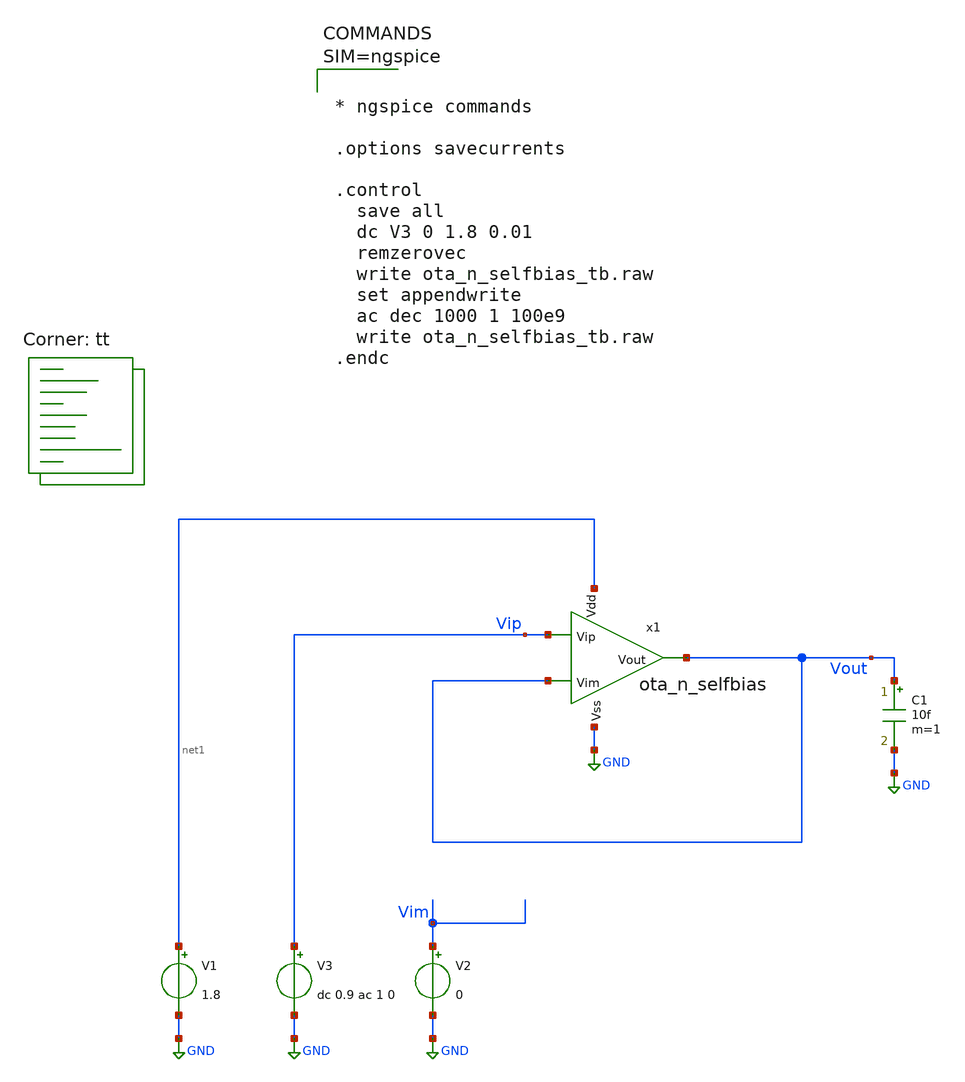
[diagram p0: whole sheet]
** sch_path: testbench/ota_n_selfbias_tb.sch
**.subckt ota_n_selfbias_tb
x1 net1 Vout Vout Vip GND ota_n_selfbias
V1 net1 GND 1.8
C1 Vout GND 10f m=1
V2 Vim GND 0
V3 Vip GND dc 0.9 ac 1 0
**** begin user architecture code
.lib $::SKYWATER_MODELS/sky130.lib.spice tt



* ngspice commands

.options savecurrents

.control
  save all
  dc V3 0 1.8 0.01
  remzerovec
  write ota_n_selfbias_tb.raw
  set appendwrite
  ac dec 1000 1 100e9
  write ota_n_selfbias_tb.raw
.endc



**** end user architecture code
**.ends

* expanding   symbol:  ota_n_selfbias.sym # of pins=5
** sym_path: schematic/ota_n_selfbias.sym
** sch_path: schematic/ota_n_selfbias.sch
.subckt ota_n_selfbias Vdd Vout Vim Vip Vss
*.ipin Vim
*.ipin Vip
*.opin Vout
*.ipin Vdd
*.ipin Vss
XM1 net1 Vim net3 Vss sky130_fd_pr__nfet_01v8_lvt L=0.4 W=1 nf=1 ad='int((1 + 1)/2) * 1 / 1 * 0.29' as='int((1 + 2)/2) * 1 / 1 * 0.29'
+ pd='2*int((1 + 1)/2) * (1 / 1 + 0.29)' ps='2*int((1 + 2)/2) * (1 / 1 + 0.29)' nrd='0.29 / 1 ' nrs='0.29 / 1 '
+ sa=0 sb=0 sd=0 mult=1 m=1
XM2 net2 Vip net3 Vss sky130_fd_pr__nfet_01v8_lvt L=0.4 W=1 nf=1 ad='int((1 + 1)/2) * 1 / 1 * 0.29' as='int((1 + 2)/2) * 1 / 1 * 0.29'
+ pd='2*int((1 + 1)/2) * (1 / 1 + 0.29)' ps='2*int((1 + 2)/2) * (1 / 1 + 0.29)' nrd='0.29 / 1 ' nrs='0.29 / 1 '
+ sa=0 sb=0 sd=0 mult=1 m=1
XM3 net3 net5 Vss Vss sky130_fd_pr__nfet_01v8_lvt L=0.4 W=1 nf=1 ad='int((1 + 1)/2) * 1 / 1 * 0.29' as='int((1 + 2)/2) * 1 / 1 * 0.29'
+ pd='2*int((1 + 1)/2) * (1 / 1 + 0.29)' ps='2*int((1 + 2)/2) * (1 / 1 + 0.29)' nrd='0.29 / 1 ' nrs='0.29 / 1 '
+ sa=0 sb=0 sd=0 mult=1 m=1
XM10 Vout net2 Vdd Vdd sky130_fd_pr__pfet_01v8_lvt L=0.4 W=1 nf=1 ad='int((1 + 1)/2) * 1 / 1 * 0.29'
+ as='int((1 + 2)/2) * 1 / 1 * 0.29' pd='2*int((1 + 1)/2) * (1 / 1 + 0.29)' ps='2*int((1 + 2)/2) * (1 / 1 + 0.29)'
+ nrd='0.29 / 1 ' nrs='0.29 / 1 ' sa=0 sb=0 sd=0 mult=1 m=1
XM4 net2 net2 Vdd Vdd sky130_fd_pr__pfet_01v8_lvt L=0.4 W=1 nf=1 ad='int((1 + 1)/2) * 1 / 1 * 0.29' as='int((1 + 2)/2) * 1 / 1 * 0.29'
+ pd='2*int((1 + 1)/2) * (1 / 1 + 0.29)' ps='2*int((1 + 2)/2) * (1 / 1 + 0.29)' nrd='0.29 / 1 ' nrs='0.29 / 1 '
+ sa=0 sb=0 sd=0 mult=1 m=1
XM5 net1 net1 Vdd Vdd sky130_fd_pr__pfet_01v8_lvt L=0.4 W=1 nf=1 ad='int((1 + 1)/2) * 1 / 1 * 0.29' as='int((1 + 2)/2) * 1 / 1 * 0.29'
+ pd='2*int((1 + 1)/2) * (1 / 1 + 0.29)' ps='2*int((1 + 2)/2) * (1 / 1 + 0.29)' nrd='0.29 / 1 ' nrs='0.29 / 1 '
+ sa=0 sb=0 sd=0 mult=1 m=1
XM7 net4 net1 Vdd Vdd sky130_fd_pr__pfet_01v8_lvt L=0.4 W=1 nf=1 ad='int((1 + 1)/2) * 1 / 1 * 0.29' as='int((1 + 2)/2) * 1 / 1 * 0.29'
+ pd='2*int((1 + 1)/2) * (1 / 1 + 0.29)' ps='2*int((1 + 2)/2) * (1 / 1 + 0.29)' nrd='0.29 / 1 ' nrs='0.29 / 1 '
+ sa=0 sb=0 sd=0 mult=1 m=1
XM6 net4 net4 Vss Vss sky130_fd_pr__nfet_01v8_lvt L=0.4 W=1 nf=1 ad='int((1 + 1)/2) * 1 / 1 * 0.29' as='int((1 + 2)/2) * 1 / 1 * 0.29'
+ pd='2*int((1 + 1)/2) * (1 / 1 + 0.29)' ps='2*int((1 + 2)/2) * (1 / 1 + 0.29)' nrd='0.29 / 1 ' nrs='0.29 / 1 '
+ sa=0 sb=0 sd=0 mult=1 m=1
XM8 Vout net4 Vss Vss sky130_fd_pr__nfet_01v8_lvt L=0.4 W=1 nf=1 ad='int((1 + 1)/2) * 1 / 1 * 0.29' as='int((1 + 2)/2) * 1 / 1 * 0.29'
+ pd='2*int((1 + 1)/2) * (1 / 1 + 0.29)' ps='2*int((1 + 2)/2) * (1 / 1 + 0.29)' nrd='0.29 / 1 ' nrs='0.29 / 1 '
+ sa=0 sb=0 sd=0 mult=1 m=1
XM9 net5 net5 Vss Vss sky130_fd_pr__nfet_01v8_lvt L=0.4 W=1 nf=1 ad='int((1 + 1)/2) * 1 / 1 * 0.29' as='int((1 + 2)/2) * 1 / 1 * 0.29'
+ pd='2*int((1 + 1)/2) * (1 / 1 + 0.29)' ps='2*int((1 + 2)/2) * (1 / 1 + 0.29)' nrd='0.29 / 1 ' nrs='0.29 / 1 '
+ sa=0 sb=0 sd=0 mult=1 m=1
XR9 net5 Vdd Vss sky130_fd_pr__res_xhigh_po W=1 L=10 mult=1 m=1
.ends

.GLOBAL GND
.end
